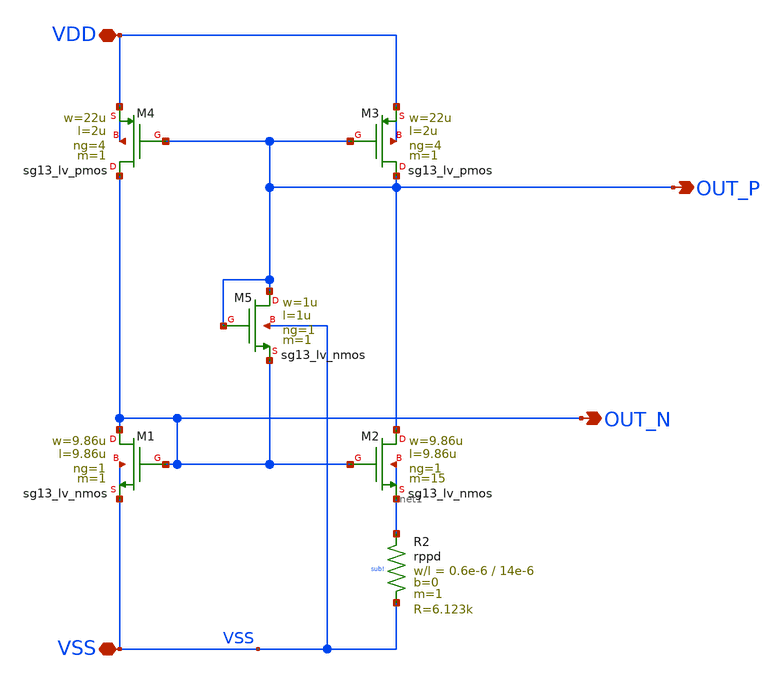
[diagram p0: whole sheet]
** sch_path: Differential_OTA_Telescopic_IHP/currentRef.sch
**.subckt currentRef VDD VSS OUT_P OUT_N
*.iopin VDD
*.iopin VSS
*.opin OUT_P
*.opin OUT_N
XM3 OUT_P OUT_P VDD VDD sg13_lv_pmos w=22u l=2u ng=4 m=1 mm_ok=1
XM2 OUT_P OUT_N net1 net1 sg13_lv_nmos w=9.86u l=9.86u ng=1 m=15 mm_ok=1
XM4 OUT_N OUT_P VDD VDD sg13_lv_pmos w=22u l=2u ng=4 m=1 mm_ok=1
XM1 OUT_N OUT_N VSS VSS sg13_lv_nmos w=9.86u l=9.86u ng=1 m=1 mm_ok=1
XM5 OUT_P OUT_P OUT_N VSS sg13_lv_nmos w=1u l=1u ng=1 m=1 mm_ok=1
XR2 net1 VSS sub! rppd w=0.6e-6 l=14e-6 m=1 b=0 mm_ok=1
**.ends
.end
